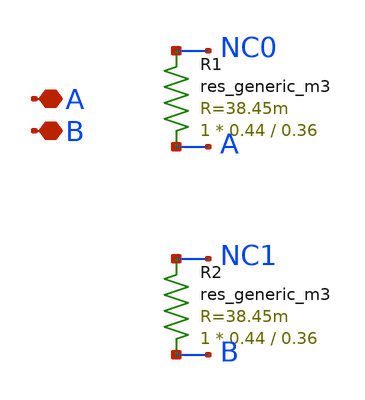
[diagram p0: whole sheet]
** sch_path: design/SUN_SAR9B_SKY130NM/SUNSAR_CAP_BSSW_CV.sch
**.subckt SUNSAR_CAP_BSSW_CV A B
*.iopin A
*.iopin B
R1 A NC0 sky130_fd_pr__res_generic_m3 W=0.44 L=0.36 m=1
R2 B NC1 sky130_fd_pr__res_generic_m3 W=0.44 L=0.36 m=1
**.ends
.end
